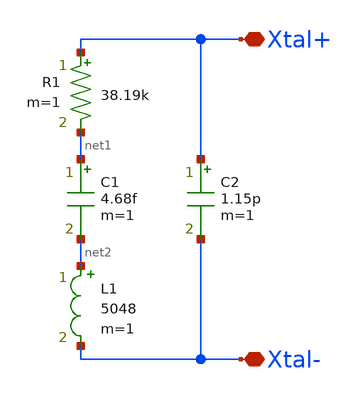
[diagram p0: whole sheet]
** sch_path: design/THESIS_EXP_RO_INVERTER_SKY130A/xtal.sch
**.subckt xtal Xtal+ Xtal-
*.iopin Xtal+
*.iopin Xtal-
R1 Xtal+ net1 38.19k m=1
C1 net1 net2 4.68f m=1
L1 net2 Xtal- 5048 m=1
C2 Xtal+ Xtal- 1.15p m=1
**.ends
.end
